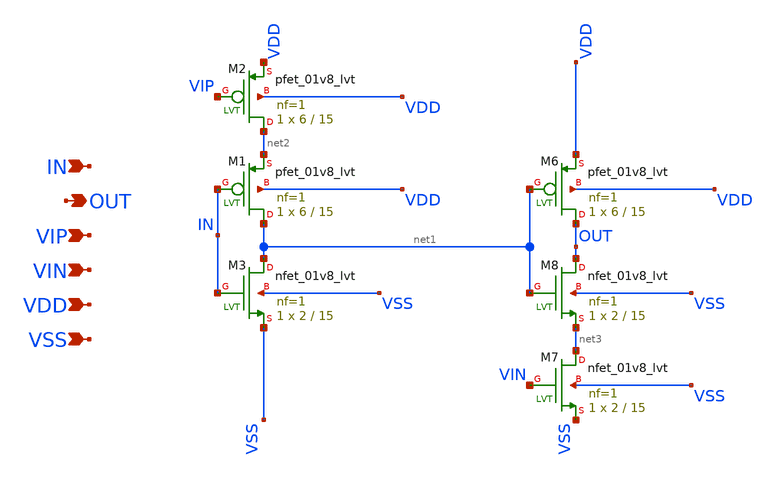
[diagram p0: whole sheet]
** sch_path: xschem/delay_element.sch
**.subckt delay_element VDD VIN IN VSS OUT VIP
*.ipin VDD
*.ipin VIN
*.ipin IN
*.ipin VSS
*.opin OUT
*.ipin VIP
XM2 net2 VIP VDD VDD sky130_fd_pr__pfet_01v8_lvt L=15 W=6 nf=1 ad='int((nf+1)/2) * W/nf * 0.29' as='int((nf+2)/2) * W/nf * 0.29'
+ pd='2*int((nf+1)/2) * (W/nf + 0.29)' ps='2*int((nf+2)/2) * (W/nf + 0.29)' nrd='0.29 / W' nrs='0.29 / W'
+ sa=0 sb=0 sd=0 mult=1 m=1
XM1 net1 IN net2 VDD sky130_fd_pr__pfet_01v8_lvt L=15 W=6 nf=1 ad='int((nf+1)/2) * W/nf * 0.29' as='int((nf+2)/2) * W/nf * 0.29'
+ pd='2*int((nf+1)/2) * (W/nf + 0.29)' ps='2*int((nf+2)/2) * (W/nf + 0.29)' nrd='0.29 / W' nrs='0.29 / W'
+ sa=0 sb=0 sd=0 mult=1 m=1
XM3 net1 IN VSS VSS sky130_fd_pr__nfet_01v8_lvt L=15 W=2 nf=1 ad='int((nf+1)/2) * W/nf * 0.29' as='int((nf+2)/2) * W/nf * 0.29'
+ pd='2*int((nf+1)/2) * (W/nf + 0.29)' ps='2*int((nf+2)/2) * (W/nf + 0.29)' nrd='0.29 / W' nrs='0.29 / W'
+ sa=0 sb=0 sd=0 mult=1 m=1
XM6 OUT net1 VDD VDD sky130_fd_pr__pfet_01v8_lvt L=15 W=6 nf=1 ad='int((nf+1)/2) * W/nf * 0.29' as='int((nf+2)/2) * W/nf * 0.29'
+ pd='2*int((nf+1)/2) * (W/nf + 0.29)' ps='2*int((nf+2)/2) * (W/nf + 0.29)' nrd='0.29 / W' nrs='0.29 / W'
+ sa=0 sb=0 sd=0 mult=1 m=1
XM8 OUT net1 net3 VSS sky130_fd_pr__nfet_01v8_lvt L=15 W=2 nf=1 ad='int((nf+1)/2) * W/nf * 0.29' as='int((nf+2)/2) * W/nf * 0.29'
+ pd='2*int((nf+1)/2) * (W/nf + 0.29)' ps='2*int((nf+2)/2) * (W/nf + 0.29)' nrd='0.29 / W' nrs='0.29 / W'
+ sa=0 sb=0 sd=0 mult=1 m=1
XM7 net3 VIN VSS VSS sky130_fd_pr__nfet_01v8_lvt L=15 W=2 nf=1 ad='int((nf+1)/2) * W/nf * 0.29' as='int((nf+2)/2) * W/nf * 0.29'
+ pd='2*int((nf+1)/2) * (W/nf + 0.29)' ps='2*int((nf+2)/2) * (W/nf + 0.29)' nrd='0.29 / W' nrs='0.29 / W'
+ sa=0 sb=0 sd=0 mult=1 m=1
**.ends
.end
